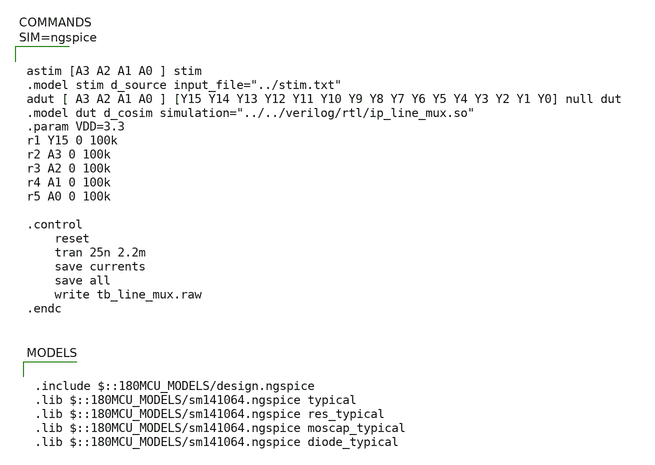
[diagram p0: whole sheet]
** sch_path: xschem/tb_line_mux.sch
**.subckt tb_line_mux
**** begin user architecture code

.include $::180MCU_MODELS/design.ngspice
.lib $::180MCU_MODELS/sm141064.ngspice typical
.lib $::180MCU_MODELS/sm141064.ngspice res_typical
.lib $::180MCU_MODELS/sm141064.ngspice moscap_typical
.lib $::180MCU_MODELS/sm141064.ngspice diode_typical




astim [A3 A2 A1 A0 ] stim
.model stim d_source input_file="../stim.txt"
adut [ A3 A2 A1 A0 ] [Y15 Y14 Y13 Y12 Y11 Y10 Y9 Y8 Y7 Y6 Y5 Y4 Y3 Y2 Y1 Y0] null dut
.model dut d_cosim simulation="../../verilog/rtl/ip_line_mux.so"
.param VDD=3.3
r1 Y15 0 100k
r2 A3 0 100k
r3 A2 0 100k
r4 A1 0 100k
r5 A0 0 100k

.control
	reset
	tran 25n 2.2m
	save currents
	save all
	write tb_line_mux.raw
.endc



**** end user architecture code
**.ends
.end
